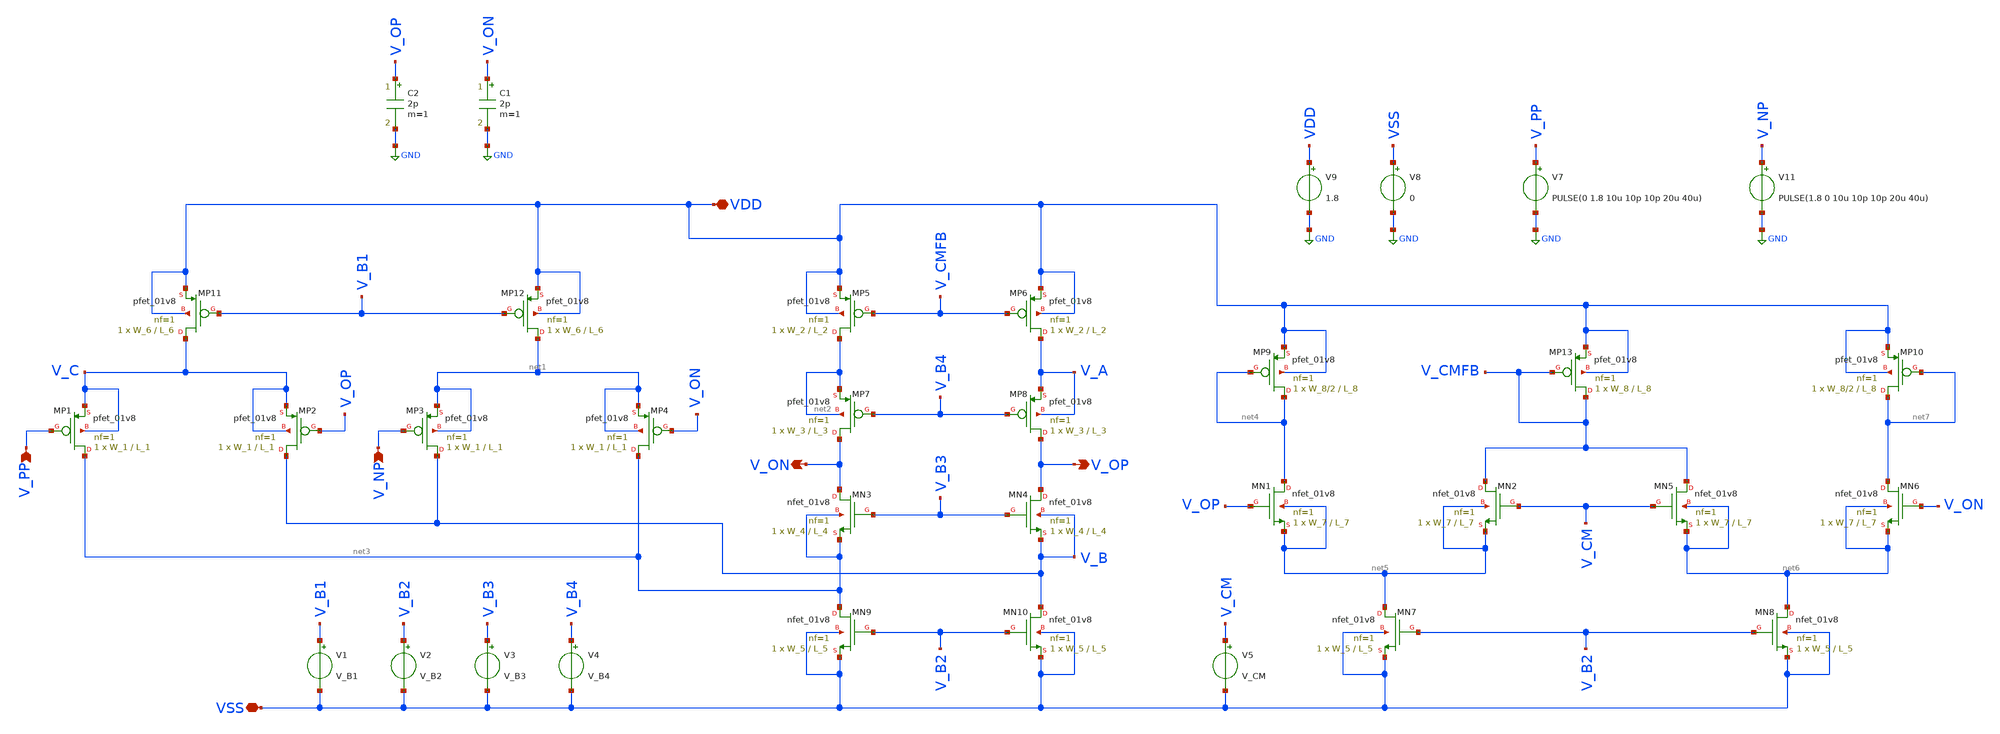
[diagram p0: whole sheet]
** sch_path: Xschem Simulations/FDDA_CMFB/tb_FDDA_CMFB_slew.sch
**.subckt tb_FDDA_CMFB_slew V_PP V_NP VDD VSS V_OP V_ON
*.ipin V_PP
*.ipin V_NP
*.iopin VDD
*.iopin VSS
*.opin V_OP
*.opin V_ON
XMP1 net3 V_PP V_C V_C sky130_fd_pr__pfet_01v8 L=L_1 W=W_1 nf=1 ad='int((1 + 1)/2) * W_1 / 1 * 0.29'
+ as='int((1 + 2)/2) * W_1 / 1 * 0.29' pd='2*int((1 + 1)/2) * (W_1 / 1 + 0.29)' ps='2*int((1 + 2)/2) * (W_1 / 1 + 0.29)'
+ nrd='0.29 / W_1 ' nrs='0.29 / W_1 ' sa=0 sb=0 sd=0 mult=1 m=1
XMP2 V_B V_OP V_C V_C sky130_fd_pr__pfet_01v8 L=L_1 W=W_1 nf=1 ad='int((1 + 1)/2) * W_1 / 1 * 0.29' as='int((1 + 2)/2) * W_1 / 1 * 0.29'
+ pd='2*int((1 + 1)/2) * (W_1 / 1 + 0.29)' ps='2*int((1 + 2)/2) * (W_1 / 1 + 0.29)' nrd='0.29 / W_1 ' nrs='0.29 / W_1 '
+ sa=0 sb=0 sd=0 mult=1 m=1
XMP3 V_B V_NP net1 net1 sky130_fd_pr__pfet_01v8 L=L_1 W=W_1 nf=1 ad='int((1 + 1)/2) * W_1 / 1 * 0.29'
+ as='int((1 + 2)/2) * W_1 / 1 * 0.29' pd='2*int((1 + 1)/2) * (W_1 / 1 + 0.29)' ps='2*int((1 + 2)/2) * (W_1 / 1 + 0.29)'
+ nrd='0.29 / W_1 ' nrs='0.29 / W_1 ' sa=0 sb=0 sd=0 mult=1 m=1
XMP4 net3 V_ON net1 net1 sky130_fd_pr__pfet_01v8 L=L_1 W=W_1 nf=1 ad='int((1 + 1)/2) * W_1 / 1 * 0.29'
+ as='int((1 + 2)/2) * W_1 / 1 * 0.29' pd='2*int((1 + 1)/2) * (W_1 / 1 + 0.29)' ps='2*int((1 + 2)/2) * (W_1 / 1 + 0.29)'
+ nrd='0.29 / W_1 ' nrs='0.29 / W_1 ' sa=0 sb=0 sd=0 mult=1 m=1
XMP5 net2 V_CMFB VDD VDD sky130_fd_pr__pfet_01v8 L=L_2 W=W_2 nf=1 ad='int((1 + 1)/2) * W_2 / 1 * 0.29'
+ as='int((1 + 2)/2) * W_2 / 1 * 0.29' pd='2*int((1 + 1)/2) * (W_2 / 1 + 0.29)' ps='2*int((1 + 2)/2) * (W_2 / 1 + 0.29)'
+ nrd='0.29 / W_2 ' nrs='0.29 / W_2 ' sa=0 sb=0 sd=0 mult=1 m=1
XMP6 V_A V_CMFB VDD VDD sky130_fd_pr__pfet_01v8 L=L_2 W=W_2 nf=1 ad='int((1 + 1)/2) * W_2 / 1 * 0.29'
+ as='int((1 + 2)/2) * W_2 / 1 * 0.29' pd='2*int((1 + 1)/2) * (W_2 / 1 + 0.29)' ps='2*int((1 + 2)/2) * (W_2 / 1 + 0.29)'
+ nrd='0.29 / W_2 ' nrs='0.29 / W_2 ' sa=0 sb=0 sd=0 mult=1 m=1
XMP7 V_ON V_B4 net2 net2 sky130_fd_pr__pfet_01v8 L=L_3 W=W_3 nf=1 ad='int((1 + 1)/2) * W_3 / 1 * 0.29'
+ as='int((1 + 2)/2) * W_3 / 1 * 0.29' pd='2*int((1 + 1)/2) * (W_3 / 1 + 0.29)' ps='2*int((1 + 2)/2) * (W_3 / 1 + 0.29)'
+ nrd='0.29 / W_3 ' nrs='0.29 / W_3 ' sa=0 sb=0 sd=0 mult=1 m=1
XMP8 V_OP V_B4 V_A V_A sky130_fd_pr__pfet_01v8 L=L_3 W=W_3 nf=1 ad='int((1 + 1)/2) * W_3 / 1 * 0.29'
+ as='int((1 + 2)/2) * W_3 / 1 * 0.29' pd='2*int((1 + 1)/2) * (W_3 / 1 + 0.29)' ps='2*int((1 + 2)/2) * (W_3 / 1 + 0.29)'
+ nrd='0.29 / W_3 ' nrs='0.29 / W_3 ' sa=0 sb=0 sd=0 mult=1 m=1
XMP11 V_C V_B1 VDD VDD sky130_fd_pr__pfet_01v8 L=L_6 W=W_6 nf=1 ad='int((1 + 1)/2) * W_6 / 1 * 0.29'
+ as='int((1 + 2)/2) * W_6 / 1 * 0.29' pd='2*int((1 + 1)/2) * (W_6 / 1 + 0.29)' ps='2*int((1 + 2)/2) * (W_6 / 1 + 0.29)'
+ nrd='0.29 / W_6 ' nrs='0.29 / W_6 ' sa=0 sb=0 sd=0 mult=1 m=1
XMP12 net1 V_B1 VDD VDD sky130_fd_pr__pfet_01v8 L=L_6 W=W_6 nf=1 ad='int((1 + 1)/2) * W_6 / 1 * 0.29'
+ as='int((1 + 2)/2) * W_6 / 1 * 0.29' pd='2*int((1 + 1)/2) * (W_6 / 1 + 0.29)' ps='2*int((1 + 2)/2) * (W_6 / 1 + 0.29)'
+ nrd='0.29 / W_6 ' nrs='0.29 / W_6 ' sa=0 sb=0 sd=0 mult=1 m=1
XMN3 V_ON V_B3 net3 net3 sky130_fd_pr__nfet_01v8 L=L_4 W=W_4 nf=1 ad='int((1 + 1)/2) * W_4 / 1 * 0.29'
+ as='int((1 + 2)/2) * W_4 / 1 * 0.29' pd='2*int((1 + 1)/2) * (W_4 / 1 + 0.29)' ps='2*int((1 + 2)/2) * (W_4 / 1 + 0.29)'
+ nrd='0.29 / W_4 ' nrs='0.29 / W_4 ' sa=0 sb=0 sd=0 mult=1 m=1
XMN4 V_OP V_B3 V_B V_B sky130_fd_pr__nfet_01v8 L=L_4 W=W_4 nf=1 ad='int((1 + 1)/2) * W_4 / 1 * 0.29'
+ as='int((1 + 2)/2) * W_4 / 1 * 0.29' pd='2*int((1 + 1)/2) * (W_4 / 1 + 0.29)' ps='2*int((1 + 2)/2) * (W_4 / 1 + 0.29)'
+ nrd='0.29 / W_4 ' nrs='0.29 / W_4 ' sa=0 sb=0 sd=0 mult=1 m=1
XMN9 net3 V_B2 VSS VSS sky130_fd_pr__nfet_01v8 L=L_5 W=W_5 nf=1 ad='int((1 + 1)/2) * W_5 / 1 * 0.29'
+ as='int((1 + 2)/2) * W_5 / 1 * 0.29' pd='2*int((1 + 1)/2) * (W_5 / 1 + 0.29)' ps='2*int((1 + 2)/2) * (W_5 / 1 + 0.29)'
+ nrd='0.29 / W_5 ' nrs='0.29 / W_5 ' sa=0 sb=0 sd=0 mult=1 m=1
XMN10 V_B V_B2 VSS VSS sky130_fd_pr__nfet_01v8 L=L_5 W=W_5 nf=1 ad='int((1 + 1)/2) * W_5 / 1 * 0.29'
+ as='int((1 + 2)/2) * W_5 / 1 * 0.29' pd='2*int((1 + 1)/2) * (W_5 / 1 + 0.29)' ps='2*int((1 + 2)/2) * (W_5 / 1 + 0.29)'
+ nrd='0.29 / W_5 ' nrs='0.29 / W_5 ' sa=0 sb=0 sd=0 mult=1 m=1
V4 V_B4 VSS V_B4
V3 V_B3 VSS V_B3
V2 V_B2 VSS V_B2
V1 V_B1 VSS V_B1
XMN1 net4 V_OP net5 net5 sky130_fd_pr__nfet_01v8 L=L_7 W=W_7 nf=1 ad='int((1 + 1)/2) * W_7 / 1 * 0.29'
+ as='int((1 + 2)/2) * W_7 / 1 * 0.29' pd='2*int((1 + 1)/2) * (W_7 / 1 + 0.29)' ps='2*int((1 + 2)/2) * (W_7 / 1 + 0.29)'
+ nrd='0.29 / W_7 ' nrs='0.29 / W_7 ' sa=0 sb=0 sd=0 mult=1 m=1
XMN2 V_CMFB V_CM net5 net5 sky130_fd_pr__nfet_01v8 L=L_7 W=W_7 nf=1 ad='int((1 + 1)/2) * W_7 / 1 * 0.29'
+ as='int((1 + 2)/2) * W_7 / 1 * 0.29' pd='2*int((1 + 1)/2) * (W_7 / 1 + 0.29)' ps='2*int((1 + 2)/2) * (W_7 / 1 + 0.29)'
+ nrd='0.29 / W_7 ' nrs='0.29 / W_7 ' sa=0 sb=0 sd=0 mult=1 m=1
XMN7 net5 V_B2 VSS VSS sky130_fd_pr__nfet_01v8 L=L_5 W=W_5 nf=1 ad='int((1 + 1)/2) * W_5 / 1 * 0.29'
+ as='int((1 + 2)/2) * W_5 / 1 * 0.29' pd='2*int((1 + 1)/2) * (W_5 / 1 + 0.29)' ps='2*int((1 + 2)/2) * (W_5 / 1 + 0.29)'
+ nrd='0.29 / W_5 ' nrs='0.29 / W_5 ' sa=0 sb=0 sd=0 mult=1 m=1
XMN6 net7 V_ON net6 net6 sky130_fd_pr__nfet_01v8 L=L_7 W=W_7 nf=1 ad='int((1 + 1)/2) * W_7 / 1 * 0.29'
+ as='int((1 + 2)/2) * W_7 / 1 * 0.29' pd='2*int((1 + 1)/2) * (W_7 / 1 + 0.29)' ps='2*int((1 + 2)/2) * (W_7 / 1 + 0.29)'
+ nrd='0.29 / W_7 ' nrs='0.29 / W_7 ' sa=0 sb=0 sd=0 mult=1 m=1
XMN5 V_CMFB V_CM net6 net6 sky130_fd_pr__nfet_01v8 L=L_7 W=W_7 nf=1 ad='int((1 + 1)/2) * W_7 / 1 * 0.29'
+ as='int((1 + 2)/2) * W_7 / 1 * 0.29' pd='2*int((1 + 1)/2) * (W_7 / 1 + 0.29)' ps='2*int((1 + 2)/2) * (W_7 / 1 + 0.29)'
+ nrd='0.29 / W_7 ' nrs='0.29 / W_7 ' sa=0 sb=0 sd=0 mult=1 m=1
XMN8 net6 V_B2 VSS VSS sky130_fd_pr__nfet_01v8 L=L_5 W=W_5 nf=1 ad='int((1 + 1)/2) * W_5 / 1 * 0.29'
+ as='int((1 + 2)/2) * W_5 / 1 * 0.29' pd='2*int((1 + 1)/2) * (W_5 / 1 + 0.29)' ps='2*int((1 + 2)/2) * (W_5 / 1 + 0.29)'
+ nrd='0.29 / W_5 ' nrs='0.29 / W_5 ' sa=0 sb=0 sd=0 mult=1 m=1
XMP9 net4 net4 VDD VDD sky130_fd_pr__pfet_01v8 L=L_8 W=W_8/2 nf=1 ad='int((1 + 1)/2) * W_8/2 / 1 * 0.29'
+ as='int((1 + 2)/2) * W_8/2 / 1 * 0.29' pd='2*int((1 + 1)/2) * (W_8/2 / 1 + 0.29)' ps='2*int((1 + 2)/2) * (W_8/2 / 1 + 0.29)'
+ nrd='0.29 / W_8/2 ' nrs='0.29 / W_8/2 ' sa=0 sb=0 sd=0 mult=1 m=1
XMP13 V_CMFB V_CMFB VDD VDD sky130_fd_pr__pfet_01v8 L=L_8 W=W_8 nf=1 ad='int((1 + 1)/2) * W_8 / 1 * 0.29'
+ as='int((1 + 2)/2) * W_8 / 1 * 0.29' pd='2*int((1 + 1)/2) * (W_8 / 1 + 0.29)' ps='2*int((1 + 2)/2) * (W_8 / 1 + 0.29)'
+ nrd='0.29 / W_8 ' nrs='0.29 / W_8 ' sa=0 sb=0 sd=0 mult=1 m=1
XMP10 net7 net7 VDD VDD sky130_fd_pr__pfet_01v8 L=L_8 W=W_8/2 nf=1 ad='int((1 + 1)/2) * W_8/2 / 1 * 0.29'
+ as='int((1 + 2)/2) * W_8/2 / 1 * 0.29' pd='2*int((1 + 1)/2) * (W_8/2 / 1 + 0.29)' ps='2*int((1 + 2)/2) * (W_8/2 / 1 + 0.29)'
+ nrd='0.29 / W_8/2 ' nrs='0.29 / W_8/2 ' sa=0 sb=0 sd=0 mult=1 m=1
V5 V_CM VSS V_CM
V7 V_PP GND PULSE(0 1.8 10u 10p 10p 20u 40u)
V8 VSS GND 0
V9 VDD GND 1.8
V11 V_NP GND PULSE(1.8 0 10u 10p 10p 20u 40u)
C1 V_ON GND 2p m=1
C2 V_OP GND 2p m=1
**** begin user architecture code

** opencircuitdesign pdks install
.lib $::SKYWATER_MODELS/sky130.lib.spice tt



.control
  save all
  tran 10n 20u

  let vin = v(v_pp) - v(v_np)
  let vout = v(v_op) - v(v_on)

  plot vin vout

  meas tran v_max FIND v(vout) AT=19u
  meas tran v_min FIND v(vout) AT=1u

  let v10 = v_min + (0.1*(v_max-v_min))
  let v90 = v_max - (0.1*(v_max-v_min))
  meas tran t10 WHEN v(vout)=v10 RISE=1
  meas tran t90 WHEN v(vout)=v90 RISE=1

  let slew_rate = ((v90 - v10) / (t90 - t10)) * 1e-6
  print slew_rate
.endc




.param temp=25
.option savecurrents
.param W_1=245.1
.param W_2=2.26
.param W_3=5.1
.param W_4=1.69
.param W_5=5.81
.param W_6=3.51
.param W_7=82.68
.param W_8=10.68
.param L_1=0.3
.param L_2=0.8
.param L_3=2
.param L_4=3
.param L_5=2
.param L_6=0.18
.param L_7=3
.param L_8=0.8
.param V_B1=0.8761
.param V_B2=0.7143
.param V_B3=1.0698
.param V_B4=0.2795
.param V_CM=0.9
.control
  save all
  op
  write tb_FDDA_CMFB_slew.raw
.endc


**** end user architecture code
**.ends
.GLOBAL GND
.end
